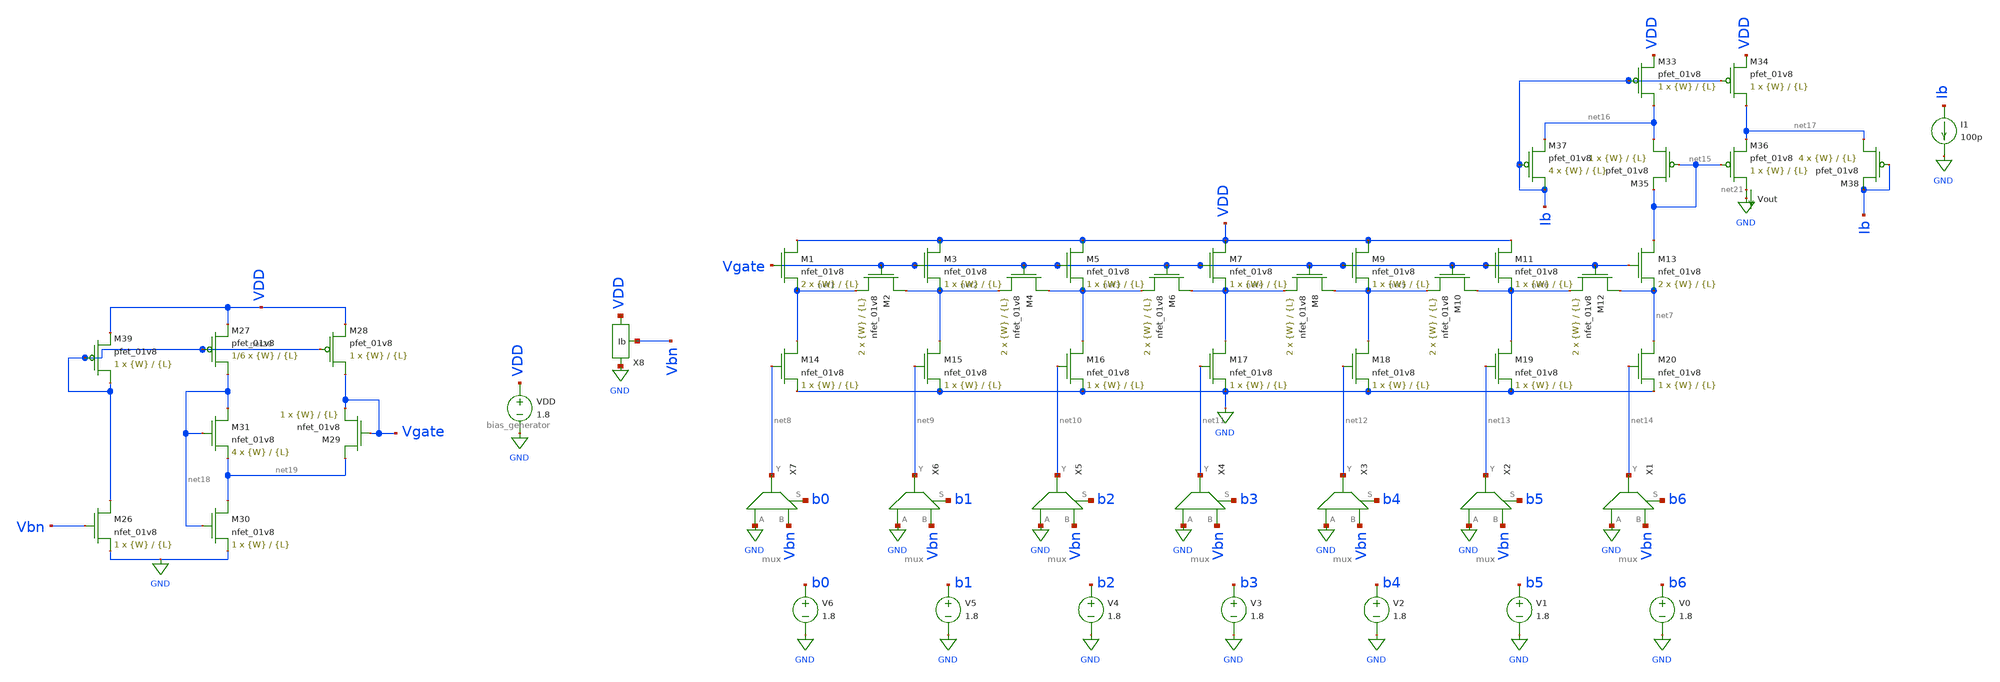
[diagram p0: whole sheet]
** sch_path: schematics/dac_output_current_current_mirror.sch
**.subckt dac_output_current_current_mirror
XM1 VDD Vgate net1 GND sky130_fd_pr__nfet_01v8 L={L} W={W} nf=1 ad='int((nf+1)/2) * W/nf * 0.29' as='int((nf+2)/2) * W/nf * 0.29'
+ pd='2*int((nf+1)/2) * (W/nf + 0.29)' ps='2*int((nf+2)/2) * (W/nf + 0.29)' nrd='0.29 / W' nrs='0.29 / W'
+ sa=0 sb=0 sd=0 mult=2 m=2
XM2 net2 Vgate net1 GND sky130_fd_pr__nfet_01v8 L={L} W={W} nf=1 ad='int((nf+1)/2) * W/nf * 0.29' as='int((nf+2)/2) * W/nf * 0.29'
+ pd='2*int((nf+1)/2) * (W/nf + 0.29)' ps='2*int((nf+2)/2) * (W/nf + 0.29)' nrd='0.29 / W' nrs='0.29 / W'
+ sa=0 sb=0 sd=0 mult=2 m=2
XM3 VDD Vgate net2 GND sky130_fd_pr__nfet_01v8 L={L} W={W} nf=1 ad='int((nf+1)/2) * W/nf * 0.29' as='int((nf+2)/2) * W/nf * 0.29'
+ pd='2*int((nf+1)/2) * (W/nf + 0.29)' ps='2*int((nf+2)/2) * (W/nf + 0.29)' nrd='0.29 / W' nrs='0.29 / W'
+ sa=0 sb=0 sd=0 mult=1 m=1
XM4 net3 Vgate net2 GND sky130_fd_pr__nfet_01v8 L={L} W={W} nf=1 ad='int((nf+1)/2) * W/nf * 0.29' as='int((nf+2)/2) * W/nf * 0.29'
+ pd='2*int((nf+1)/2) * (W/nf + 0.29)' ps='2*int((nf+2)/2) * (W/nf + 0.29)' nrd='0.29 / W' nrs='0.29 / W'
+ sa=0 sb=0 sd=0 mult=2 m=2
XM5 VDD Vgate net3 GND sky130_fd_pr__nfet_01v8 L={L} W={W} nf=1 ad='int((nf+1)/2) * W/nf * 0.29' as='int((nf+2)/2) * W/nf * 0.29'
+ pd='2*int((nf+1)/2) * (W/nf + 0.29)' ps='2*int((nf+2)/2) * (W/nf + 0.29)' nrd='0.29 / W' nrs='0.29 / W'
+ sa=0 sb=0 sd=0 mult=1 m=1
XM6 net4 Vgate net3 GND sky130_fd_pr__nfet_01v8 L={L} W={W} nf=1 ad='int((nf+1)/2) * W/nf * 0.29' as='int((nf+2)/2) * W/nf * 0.29'
+ pd='2*int((nf+1)/2) * (W/nf + 0.29)' ps='2*int((nf+2)/2) * (W/nf + 0.29)' nrd='0.29 / W' nrs='0.29 / W'
+ sa=0 sb=0 sd=0 mult=2 m=2
XM7 VDD Vgate net4 GND sky130_fd_pr__nfet_01v8 L={L} W={W} nf=1 ad='int((nf+1)/2) * W/nf * 0.29' as='int((nf+2)/2) * W/nf * 0.29'
+ pd='2*int((nf+1)/2) * (W/nf + 0.29)' ps='2*int((nf+2)/2) * (W/nf + 0.29)' nrd='0.29 / W' nrs='0.29 / W'
+ sa=0 sb=0 sd=0 mult=1 m=1
XM8 net5 Vgate net4 GND sky130_fd_pr__nfet_01v8 L={L} W={W} nf=1 ad='int((nf+1)/2) * W/nf * 0.29' as='int((nf+2)/2) * W/nf * 0.29'
+ pd='2*int((nf+1)/2) * (W/nf + 0.29)' ps='2*int((nf+2)/2) * (W/nf + 0.29)' nrd='0.29 / W' nrs='0.29 / W'
+ sa=0 sb=0 sd=0 mult=2 m=2
XM9 VDD Vgate net5 GND sky130_fd_pr__nfet_01v8 L={L} W={W} nf=1 ad='int((nf+1)/2) * W/nf * 0.29' as='int((nf+2)/2) * W/nf * 0.29'
+ pd='2*int((nf+1)/2) * (W/nf + 0.29)' ps='2*int((nf+2)/2) * (W/nf + 0.29)' nrd='0.29 / W' nrs='0.29 / W'
+ sa=0 sb=0 sd=0 mult=1 m=1
XM10 net6 Vgate net5 GND sky130_fd_pr__nfet_01v8 L={L} W={W} nf=1 ad='int((nf+1)/2) * W/nf * 0.29' as='int((nf+2)/2) * W/nf * 0.29'
+ pd='2*int((nf+1)/2) * (W/nf + 0.29)' ps='2*int((nf+2)/2) * (W/nf + 0.29)' nrd='0.29 / W' nrs='0.29 / W'
+ sa=0 sb=0 sd=0 mult=2 m=2
XM11 VDD Vgate net6 GND sky130_fd_pr__nfet_01v8 L={L} W={W} nf=1 ad='int((nf+1)/2) * W/nf * 0.29' as='int((nf+2)/2) * W/nf * 0.29'
+ pd='2*int((nf+1)/2) * (W/nf + 0.29)' ps='2*int((nf+2)/2) * (W/nf + 0.29)' nrd='0.29 / W' nrs='0.29 / W'
+ sa=0 sb=0 sd=0 mult=1 m=1
XM12 net7 Vgate net6 GND sky130_fd_pr__nfet_01v8 L={L} W={W} nf=1 ad='int((nf+1)/2) * W/nf * 0.29' as='int((nf+2)/2) * W/nf * 0.29'
+ pd='2*int((nf+1)/2) * (W/nf + 0.29)' ps='2*int((nf+2)/2) * (W/nf + 0.29)' nrd='0.29 / W' nrs='0.29 / W'
+ sa=0 sb=0 sd=0 mult=2 m=2
XM13 net15 Vgate net7 GND sky130_fd_pr__nfet_01v8 L={L} W={W} nf=1 ad='int((nf+1)/2) * W/nf * 0.29' as='int((nf+2)/2) * W/nf * 0.29'
+ pd='2*int((nf+1)/2) * (W/nf + 0.29)' ps='2*int((nf+2)/2) * (W/nf + 0.29)' nrd='0.29 / W' nrs='0.29 / W'
+ sa=0 sb=0 sd=0 mult=2 m=2
XM14 net1 net8 GND GND sky130_fd_pr__nfet_01v8 L={L} W={W} nf=1 ad='int((nf+1)/2) * W/nf * 0.29' as='int((nf+2)/2) * W/nf * 0.29'
+ pd='2*int((nf+1)/2) * (W/nf + 0.29)' ps='2*int((nf+2)/2) * (W/nf + 0.29)' nrd='0.29 / W' nrs='0.29 / W'
+ sa=0 sb=0 sd=0 mult=1 m=1
XM15 net2 net9 GND GND sky130_fd_pr__nfet_01v8 L={L} W={W} nf=1 ad='int((nf+1)/2) * W/nf * 0.29' as='int((nf+2)/2) * W/nf * 0.29'
+ pd='2*int((nf+1)/2) * (W/nf + 0.29)' ps='2*int((nf+2)/2) * (W/nf + 0.29)' nrd='0.29 / W' nrs='0.29 / W'
+ sa=0 sb=0 sd=0 mult=1 m=1
XM16 net3 net10 GND GND sky130_fd_pr__nfet_01v8 L={L} W={W} nf=1 ad='int((nf+1)/2) * W/nf * 0.29' as='int((nf+2)/2) * W/nf * 0.29'
+ pd='2*int((nf+1)/2) * (W/nf + 0.29)' ps='2*int((nf+2)/2) * (W/nf + 0.29)' nrd='0.29 / W' nrs='0.29 / W'
+ sa=0 sb=0 sd=0 mult=1 m=1
XM17 net4 net11 GND GND sky130_fd_pr__nfet_01v8 L={L} W={W} nf=1 ad='int((nf+1)/2) * W/nf * 0.29' as='int((nf+2)/2) * W/nf * 0.29'
+ pd='2*int((nf+1)/2) * (W/nf + 0.29)' ps='2*int((nf+2)/2) * (W/nf + 0.29)' nrd='0.29 / W' nrs='0.29 / W'
+ sa=0 sb=0 sd=0 mult=1 m=1
XM18 net5 net12 GND GND sky130_fd_pr__nfet_01v8 L={L} W={W} nf=1 ad='int((nf+1)/2) * W/nf * 0.29' as='int((nf+2)/2) * W/nf * 0.29'
+ pd='2*int((nf+1)/2) * (W/nf + 0.29)' ps='2*int((nf+2)/2) * (W/nf + 0.29)' nrd='0.29 / W' nrs='0.29 / W'
+ sa=0 sb=0 sd=0 mult=1 m=1
XM19 net6 net13 GND GND sky130_fd_pr__nfet_01v8 L={L} W={W} nf=1 ad='int((nf+1)/2) * W/nf * 0.29' as='int((nf+2)/2) * W/nf * 0.29'
+ pd='2*int((nf+1)/2) * (W/nf + 0.29)' ps='2*int((nf+2)/2) * (W/nf + 0.29)' nrd='0.29 / W' nrs='0.29 / W'
+ sa=0 sb=0 sd=0 mult=1 m=1
XM20 net7 net14 GND GND sky130_fd_pr__nfet_01v8 L={L} W={W} nf=1 ad='int((nf+1)/2) * W/nf * 0.29' as='int((nf+2)/2) * W/nf * 0.29'
+ pd='2*int((nf+1)/2) * (W/nf + 0.29)' ps='2*int((nf+2)/2) * (W/nf + 0.29)' nrd='0.29 / W' nrs='0.29 / W'
+ sa=0 sb=0 sd=0 mult=1 m=1
X1 GND Vbn net14 b6 mux
X2 GND Vbn net13 b5 mux
X3 GND Vbn net12 b4 mux
X4 GND Vbn net11 b3 mux
X5 GND Vbn net10 b2 mux
X6 GND Vbn net9 b1 mux
X7 GND Vbn net8 b0 mux
V0 b6 GND 1.8
V1 b5 GND 1.8
V2 b4 GND 1.8
V3 b3 GND 1.8
V4 b2 GND 1.8
V5 b1 GND 1.8
V6 b0 GND 1.8
Vout net21 GND 0
.save i(vout)
VDD VDD GND 1.8
X8 VDD GND Vbn bias_generator
XM33 net16 Ib VDD VDD sky130_fd_pr__pfet_01v8 L={L} W={W} nf=1 ad='int((nf+1)/2) * W/nf * 0.29' as='int((nf+2)/2) * W/nf * 0.29'
+ pd='2*int((nf+1)/2) * (W/nf + 0.29)' ps='2*int((nf+2)/2) * (W/nf + 0.29)' nrd='0.29 / W' nrs='0.29 / W'
+ sa=0 sb=0 sd=0 mult=1 m=1
XM34 net17 Ib VDD VDD sky130_fd_pr__pfet_01v8 L={L} W={W} nf=1 ad='int((nf+1)/2) * W/nf * 0.29' as='int((nf+2)/2) * W/nf * 0.29'
+ pd='2*int((nf+1)/2) * (W/nf + 0.29)' ps='2*int((nf+2)/2) * (W/nf + 0.29)' nrd='0.29 / W' nrs='0.29 / W'
+ sa=0 sb=0 sd=0 mult=1 m=1
XM35 net16 net15 net15 VDD sky130_fd_pr__pfet_01v8 L={L} W={W} nf=1 ad='int((nf+1)/2) * W/nf * 0.29'
+ as='int((nf+2)/2) * W/nf * 0.29' pd='2*int((nf+1)/2) * (W/nf + 0.29)' ps='2*int((nf+2)/2) * (W/nf + 0.29)'
+ nrd='0.29 / W' nrs='0.29 / W' sa=0 sb=0 sd=0 mult=1 m=1
XM36 net21 net15 net17 VDD sky130_fd_pr__pfet_01v8 L={L} W={W} nf=1 ad='int((nf+1)/2) * W/nf * 0.29'
+ as='int((nf+2)/2) * W/nf * 0.29' pd='2*int((nf+1)/2) * (W/nf + 0.29)' ps='2*int((nf+2)/2) * (W/nf + 0.29)'
+ nrd='0.29 / W' nrs='0.29 / W' sa=0 sb=0 sd=0 mult=1 m=1
XM37 Ib Ib net16 VDD sky130_fd_pr__pfet_01v8 L={L} W={W} nf=1 ad='int((nf+1)/2) * W/nf * 0.29' as='int((nf+2)/2) * W/nf * 0.29'
+ pd='2*int((nf+1)/2) * (W/nf + 0.29)' ps='2*int((nf+2)/2) * (W/nf + 0.29)' nrd='0.29 / W' nrs='0.29 / W'
+ sa=0 sb=0 sd=0 mult=4 m=4
XM38 net17 Ib Ib VDD sky130_fd_pr__pfet_01v8 L={L} W={W} nf=1 ad='int((nf+1)/2) * W/nf * 0.29' as='int((nf+2)/2) * W/nf * 0.29'
+ pd='2*int((nf+1)/2) * (W/nf + 0.29)' ps='2*int((nf+2)/2) * (W/nf + 0.29)' nrd='0.29 / W' nrs='0.29 / W'
+ sa=0 sb=0 sd=0 mult=4 m=4
I1 Ib GND 100p
XM26 net20 Vbn GND GND sky130_fd_pr__nfet_01v8 L={L} W={W} nf=1 ad='int((nf+1)/2) * W/nf * 0.29' as='int((nf+2)/2) * W/nf * 0.29'
+ pd='2*int((nf+1)/2) * (W/nf + 0.29)' ps='2*int((nf+2)/2) * (W/nf + 0.29)' nrd='0.29 / W' nrs='0.29 / W'
+ sa=0 sb=0 sd=0 mult=1 m=1
XM27 net18 net20 VDD VDD sky130_fd_pr__pfet_01v8 L={L} W={W} nf=1 ad='int((nf+1)/2) * W/nf * 0.29' as='int((nf+2)/2) * W/nf * 0.29'
+ pd='2*int((nf+1)/2) * (W/nf + 0.29)' ps='2*int((nf+2)/2) * (W/nf + 0.29)' nrd='0.29 / W' nrs='0.29 / W'
+ sa=0 sb=0 sd=0 mult=1/6 m=1/6
XM28 Vgate net20 VDD VDD sky130_fd_pr__pfet_01v8 L={L} W={W} nf=1 ad='int((nf+1)/2) * W/nf * 0.29' as='int((nf+2)/2) * W/nf * 0.29'
+ pd='2*int((nf+1)/2) * (W/nf + 0.29)' ps='2*int((nf+2)/2) * (W/nf + 0.29)' nrd='0.29 / W' nrs='0.29 / W'
+ sa=0 sb=0 sd=0 mult=1 m=1
XM29 net19 Vgate Vgate GND sky130_fd_pr__nfet_01v8 L={L} W={W} nf=1 ad='int((nf+1)/2) * W/nf * 0.29'
+ as='int((nf+2)/2) * W/nf * 0.29' pd='2*int((nf+1)/2) * (W/nf + 0.29)' ps='2*int((nf+2)/2) * (W/nf + 0.29)'
+ nrd='0.29 / W' nrs='0.29 / W' sa=0 sb=0 sd=0 mult=1 m=1
XM30 net19 net18 GND GND sky130_fd_pr__nfet_01v8 L={L} W={W} nf=1 ad='int((nf+1)/2) * W/nf * 0.29' as='int((nf+2)/2) * W/nf * 0.29'
+ pd='2*int((nf+1)/2) * (W/nf + 0.29)' ps='2*int((nf+2)/2) * (W/nf + 0.29)' nrd='0.29 / W' nrs='0.29 / W'
+ sa=0 sb=0 sd=0 mult=1 m=1
XM31 net18 net18 net19 GND sky130_fd_pr__nfet_01v8 L={L} W={W} nf=1 ad='int((nf+1)/2) * W/nf * 0.29'
+ as='int((nf+2)/2) * W/nf * 0.29' pd='2*int((nf+1)/2) * (W/nf + 0.29)' ps='2*int((nf+2)/2) * (W/nf + 0.29)'
+ nrd='0.29 / W' nrs='0.29 / W' sa=0 sb=0 sd=0 mult=4 m=4
XM39 net20 net20 VDD VDD sky130_fd_pr__pfet_01v8 L={L} W={W} nf=1 ad='int((nf+1)/2) * W/nf * 0.29' as='int((nf+2)/2) * W/nf * 0.29'
+ pd='2*int((nf+1)/2) * (W/nf + 0.29)' ps='2*int((nf+2)/2) * (W/nf + 0.29)' nrd='0.29 / W' nrs='0.29 / W'
+ sa=0 sb=0 sd=0 mult=1 m=1
**** begin user architecture code

.param W=1
.param L=0.5
.dc VDD 0 1.8 0.01
.save i(Vout) v(VDD) v(Vbn)


.option wnflag=1
.param MC_SWITCH=0.0
.lib ~/skywater/skywater-pdk/libraries/sky130_fd_pr_ngspice/latest/models/sky130.lib.spice tt

**** end user architecture code
**.ends

* expanding   symbol:  /home/madvlsi/Documents/current-output-dac-vlsi/schematics/mux.sym # of
*+ pins=4
** sym_path: /home/madvlsi/Documents/current-output-dac-vlsi/schematics/mux.sym
** sch_path: /home/madvlsi/Documents/current-output-dac-vlsi/schematics/mux.sch
.subckt mux A B Y S
*.ipin S
*.ipin A
*.opin Y
*.ipin B
XM1 net1 S GND GND sky130_fd_pr__nfet_01v8 L=0.15 W=1 nf=1 ad='int((nf+1)/2) * W/nf * 0.29' as='int((nf+2)/2) * W/nf * 0.29'
+ pd='2*int((nf+1)/2) * (W/nf + 0.29)' ps='2*int((nf+2)/2) * (W/nf + 0.29)' nrd='0.29 / W' nrs='0.29 / W'
+ sa=0 sb=0 sd=0 mult=1 m=1
XM2 net1 S VDD VDD sky130_fd_pr__pfet_01v8 L=0.15 W=1 nf=1 ad='int((nf+1)/2) * W/nf * 0.29' as='int((nf+2)/2) * W/nf * 0.29'
+ pd='2*int((nf+1)/2) * (W/nf + 0.29)' ps='2*int((nf+2)/2) * (W/nf + 0.29)' nrd='0.29 / W' nrs='0.29 / W'
+ sa=0 sb=0 sd=0 mult=1 m=1
XM3 Y S B GND sky130_fd_pr__nfet_01v8 L=0.15 W=1 nf=1 ad='int((nf+1)/2) * W/nf * 0.29' as='int((nf+2)/2) * W/nf * 0.29'
+ pd='2*int((nf+1)/2) * (W/nf + 0.29)' ps='2*int((nf+2)/2) * (W/nf + 0.29)' nrd='0.29 / W' nrs='0.29 / W'
+ sa=0 sb=0 sd=0 mult=1 m=1
XM4 A net1 Y GND sky130_fd_pr__nfet_01v8 L=0.15 W=1 nf=1 ad='int((nf+1)/2) * W/nf * 0.29' as='int((nf+2)/2) * W/nf * 0.29'
+ pd='2*int((nf+1)/2) * (W/nf + 0.29)' ps='2*int((nf+2)/2) * (W/nf + 0.29)' nrd='0.29 / W' nrs='0.29 / W'
+ sa=0 sb=0 sd=0 mult=1 m=1
.ends


* expanding   symbol:  /home/madvlsi/Documents/current-output-dac-vlsi/schematics/bias_generator.sym
*+ # of pins=3
** sym_path: schematics/bias_generator.sym
** sch_path: schematics/bias_generator.sch
.subckt bias_generator VP VN Ib
*.iopin VP
*.iopin VN
*.opin Ib
XM2 VP net2 net4 VDD sky130_fd_pr__pfet_01v8 L=0.15 W=1 nf=1 ad='int((nf+1)/2) * W/nf * 0.29' as='int((nf+2)/2) * W/nf * 0.29'
+ pd='2*int((nf+1)/2) * (W/nf + 0.29)' ps='2*int((nf+2)/2) * (W/nf + 0.29)' nrd='0.29 / W' nrs='0.29 / W'
+ sa=0 sb=0 sd=0 mult=1 m=1
XM1 VP net1 net1 VDD sky130_fd_pr__pfet_01v8 L=0.15 W=1 nf=1 ad='int((nf+1)/2) * W/nf * 0.29' as='int((nf+2)/2) * W/nf * 0.29'
+ pd='2*int((nf+1)/2) * (W/nf + 0.29)' ps='2*int((nf+2)/2) * (W/nf + 0.29)' nrd='0.29 / W' nrs='0.29 / W'
+ sa=0 sb=0 sd=0 mult=1 m=1
XM3 net2 net1 VP VDD sky130_fd_pr__pfet_01v8 L=0.15 W=1 nf=1 ad='int((nf+1)/2) * W/nf * 0.29' as='int((nf+2)/2) * W/nf * 0.29'
+ pd='2*int((nf+1)/2) * (W/nf + 0.29)' ps='2*int((nf+2)/2) * (W/nf + 0.29)' nrd='0.29 / W' nrs='0.29 / W'
+ sa=0 sb=0 sd=0 mult=1 m=1
XM4 net3 net2 VP VDD sky130_fd_pr__pfet_01v8 L=0.15 W=1 nf=1 ad='int((nf+1)/2) * W/nf * 0.29' as='int((nf+2)/2) * W/nf * 0.29'
+ pd='2*int((nf+1)/2) * (W/nf + 0.29)' ps='2*int((nf+2)/2) * (W/nf + 0.29)' nrd='0.29 / W' nrs='0.29 / W'
+ sa=0 sb=0 sd=0 mult=1 m=1
XM5 net6 net4 net4 GND sky130_fd_pr__nfet_01v8 L=0.15 W=1 nf=1 ad='int((nf+1)/2) * W/nf * 0.29' as='int((nf+2)/2) * W/nf * 0.29'
+ pd='2*int((nf+1)/2) * (W/nf + 0.29)' ps='2*int((nf+2)/2) * (W/nf + 0.29)' nrd='0.29 / W' nrs='0.29 / W'
+ sa=0 sb=0 sd=0 mult=1 m=1
XM6 net1 net4 VN GND sky130_fd_pr__nfet_01v8 L=0.15 W=1 nf=1 ad='int((nf+1)/2) * W/nf * 0.29' as='int((nf+2)/2) * W/nf * 0.29'
+ pd='2*int((nf+1)/2) * (W/nf + 0.29)' ps='2*int((nf+2)/2) * (W/nf + 0.29)' nrd='0.29 / W' nrs='0.29 / W'
+ sa=0 sb=0 sd=0 mult=1 m=1
XM7 VN net3 net2 GND sky130_fd_pr__nfet_01v8 L=0.15 W=1 nf=1 ad='int((nf+1)/2) * W/nf * 0.29' as='int((nf+2)/2) * W/nf * 0.29'
+ pd='2*int((nf+1)/2) * (W/nf + 0.29)' ps='2*int((nf+2)/2) * (W/nf + 0.29)' nrd='0.29 / W' nrs='0.29 / W'
+ sa=0 sb=0 sd=0 mult=1 m=1
XM8 net3 net3 VN GND sky130_fd_pr__nfet_01v8 L=0.15 W=1 nf=1 ad='int((nf+1)/2) * W/nf * 0.29' as='int((nf+2)/2) * W/nf * 0.29'
+ pd='2*int((nf+1)/2) * (W/nf + 0.29)' ps='2*int((nf+2)/2) * (W/nf + 0.29)' nrd='0.29 / W' nrs='0.29 / W'
+ sa=0 sb=0 sd=0 mult=1 m=1
R1 net6 VN 100 m=1
XM9 net5 net3 VN GND sky130_fd_pr__nfet_01v8 L=0.15 W=1 nf=1 ad='int((nf+1)/2) * W/nf * 0.29' as='int((nf+2)/2) * W/nf * 0.29'
+ pd='2*int((nf+1)/2) * (W/nf + 0.29)' ps='2*int((nf+2)/2) * (W/nf + 0.29)' nrd='0.29 / W' nrs='0.29 / W'
+ sa=0 sb=0 sd=0 mult=1 m=1
XM10 VP net5 net5 VDD sky130_fd_pr__pfet_01v8 L=0.15 W=1 nf=1 ad='int((nf+1)/2) * W/nf * 0.29' as='int((nf+2)/2) * W/nf * 0.29'
+ pd='2*int((nf+1)/2) * (W/nf + 0.29)' ps='2*int((nf+2)/2) * (W/nf + 0.29)' nrd='0.29 / W' nrs='0.29 / W'
+ sa=0 sb=0 sd=0 mult=1 m=1
XM11 Ib net5 VP VDD sky130_fd_pr__pfet_01v8 L=0.15 W=1 nf=1 ad='int((nf+1)/2) * W/nf * 0.29' as='int((nf+2)/2) * W/nf * 0.29'
+ pd='2*int((nf+1)/2) * (W/nf + 0.29)' ps='2*int((nf+2)/2) * (W/nf + 0.29)' nrd='0.29 / W' nrs='0.29 / W'
+ sa=0 sb=0 sd=0 mult=1 m=1
.ends

.GLOBAL GND
.GLOBAL VDD
.end
